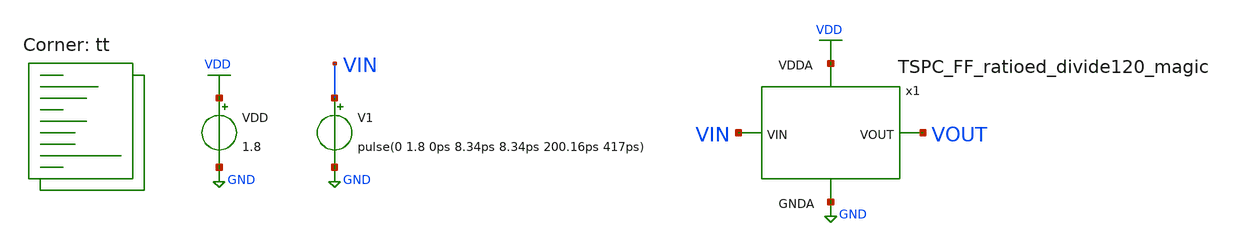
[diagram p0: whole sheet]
** sch_path: projects/pll/divider/magic/divide_by_120/tb_TSPC_FF_ratioed_divide120_magic.sch
**.subckt tb_TSPC_FF_ratioed_divide120_magic
VDD VDD GND 1.8
V1 VIN GND pulse(0 1.8 0ps 8.34ps 8.34ps 200.16ps 417ps)
x1 VOUT VIN VDD GND TSPC_FF_ratioed_divide120_magic
**** begin user architecture code



.include /foss/designs/my_design/projects/pll/divider/magic/divide_by_120/TSPC_FF_ratioed_divide120_magic.spice

.option method=gear
.option wnflag=1

.control

  save all
  tran 5p 200n
  remzerovec
  write tb_TSPC_FF_ratioed_divide120_magic.raw
  set appendwrite
.endc



.lib $::SKYWATER_MODELS/sky130.lib.spice tt
**** end user architecture code
**.ends
.GLOBAL GND
.GLOBAL VDD
.end
